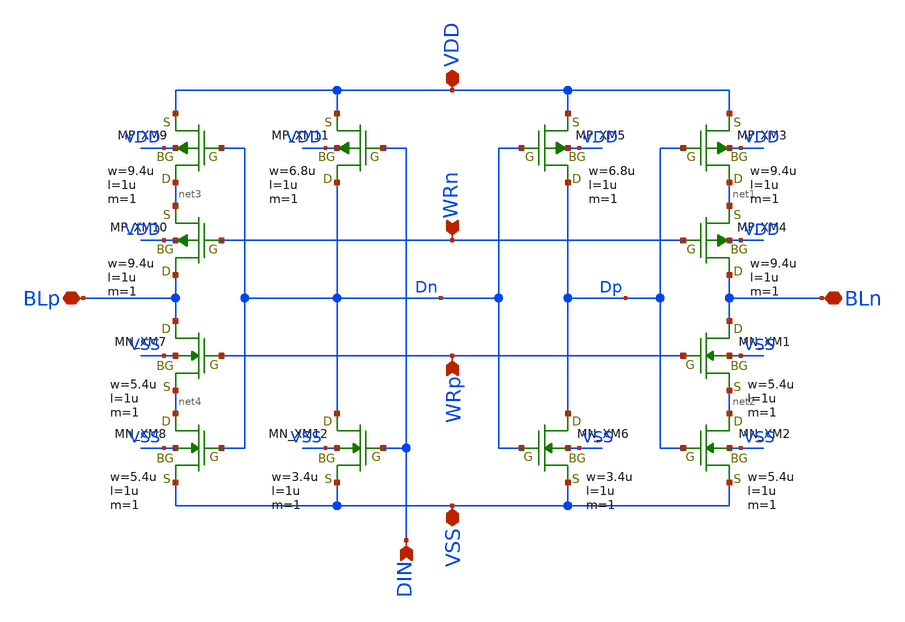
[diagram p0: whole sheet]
** sch_path: module/SRAM128/schematic/WDRV.sch
**.subckt WDRV BLn BLp DIN WRn WRp VDD VSS
*.iopin BLn
*.iopin BLp
*.ipin DIN
*.ipin WRn
*.ipin WRp
*.iopin VDD
*.iopin VSS
XXM1 BLn WRp net2 VSS NMOS w=5.4u l=1u as=0 ad=0 ps=0 pd=0 nrd=0 nrs=0 m=1
XXM2 net2 Dp VSS VSS NMOS w=5.4u l=1u as=0 ad=0 ps=0 pd=0 nrd=0 nrs=0 m=1
XXM3 net1 Dp VDD VDD PMOS w=9.4u l=1u as=0 ad=0 ps=0 pd=0 nrd=0 nrs=0 m=1
XXM4 BLn WRn net1 VDD PMOS w=9.4u l=1u as=0 ad=0 ps=0 pd=0 nrd=0 nrs=0 m=1
XXM5 Dp Dn VDD VDD PMOS w=6.8u l=1u as=0 ad=0 ps=0 pd=0 nrd=0 nrs=0 m=1
XXM6 Dp Dn VSS VSS NMOS w=3.4u l=1u as=0 ad=0 ps=0 pd=0 nrd=0 nrs=0 m=1
XXM7 BLp WRp net4 VSS NMOS w=5.4u l=1u as=0 ad=0 ps=0 pd=0 nrd=0 nrs=0 m=1
XXM8 net4 Dn VSS VSS NMOS w=5.4u l=1u as=0 ad=0 ps=0 pd=0 nrd=0 nrs=0 m=1
XXM9 net3 Dn VDD VDD PMOS w=9.4u l=1u as=0 ad=0 ps=0 pd=0 nrd=0 nrs=0 m=1
XXM10 BLp WRn net3 VDD PMOS w=9.4u l=1u as=0 ad=0 ps=0 pd=0 nrd=0 nrs=0 m=1
XXM11 Dn DIN VDD VDD PMOS w=6.8u l=1u as=0 ad=0 ps=0 pd=0 nrd=0 nrs=0 m=1
XXM12 Dn DIN VSS VSS NMOS w=3.4u l=1u as=0 ad=0 ps=0 pd=0 nrd=0 nrs=0 m=1
**.ends
.end
